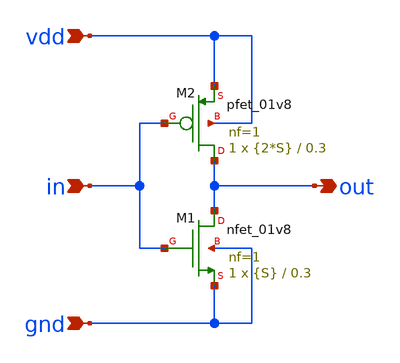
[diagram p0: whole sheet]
** sch_path: xsch/cc_inv_dt.sch
**.subckt cc_inv_dt in vdd gnd out
*.ipin in
*.ipin vdd
*.ipin gnd
*.opin out
XM1 out in gnd gnd sky130_fd_pr__nfet_01v8 L=0.3 W={S} nf=1 ad='int((nf+1)/2) * W/nf * 0.29' as='int((nf+2)/2) * W/nf * 0.29'
+ pd='2*int((nf+1)/2) * (W/nf + 0.29)' ps='2*int((nf+2)/2) * (W/nf + 0.29)' nrd='0.29 / W' nrs='0.29 / W'
+ sa=0 sb=0 sd=0 mult=1 m=1
XM2 out in vdd vdd sky130_fd_pr__pfet_01v8 L=0.3 W={2*S} nf=1 ad='int((nf+1)/2) * W/nf * 0.29' as='int((nf+2)/2) * W/nf * 0.29'
+ pd='2*int((nf+1)/2) * (W/nf + 0.29)' ps='2*int((nf+2)/2) * (W/nf + 0.29)' nrd='0.29 / W' nrs='0.29 / W'
+ sa=0 sb=0 sd=0 mult=1 m=1
**.ends
.end
